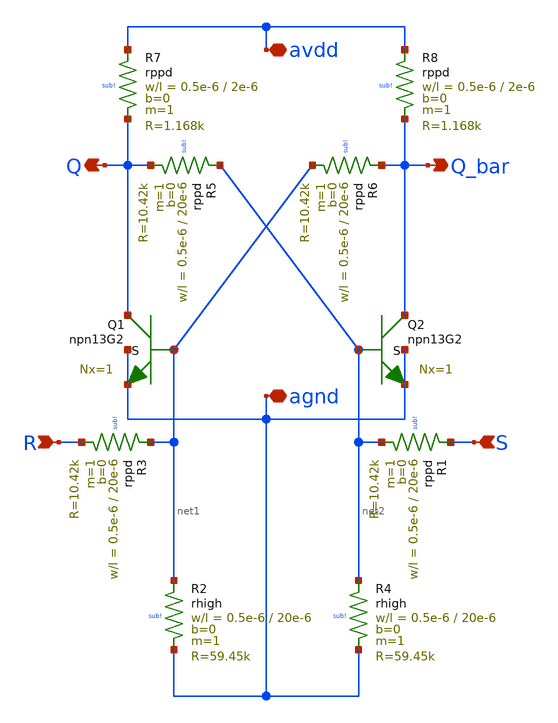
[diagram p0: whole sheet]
** sch_path: xschem/SR_latch.sch
**.subckt SR_latch R Q_bar S Q avdd agnd
*.ipin R
*.opin Q_bar
*.ipin S
*.opin Q
*.iopin avdd
*.iopin agnd
XQ2 Q_bar net2 agnd agnd npn13G2 Nx=1 mm_ok=1
XQ1 Q net1 agnd agnd npn13G2 Nx=1 mm_ok=1
XR3 net1 R sub! rppd w=0.5e-6 l=20e-6 m=1 b=0 mm_ok=1
XR1 S net2 sub! rppd w=0.5e-6 l=20e-6 m=1 b=0 mm_ok=1
XR2 net1 agnd sub! rhigh w=0.5e-6 l=20e-6 m=1 b=0 mm_ok=1
XR4 net2 agnd sub! rhigh w=0.5e-6 l=20e-6 m=1 b=0 mm_ok=1
XR5 net2 Q sub! rppd w=0.5e-6 l=20e-6 m=1 b=0 mm_ok=1
XR6 Q_bar net1 sub! rppd w=0.5e-6 l=20e-6 m=1 b=0 mm_ok=1
XR7 avdd Q sub! rppd w=0.5e-6 l=2e-6 m=1 b=0 mm_ok=1
XR8 avdd Q_bar sub! rppd w=0.5e-6 l=2e-6 m=1 b=0 mm_ok=1
**.ends
.end
